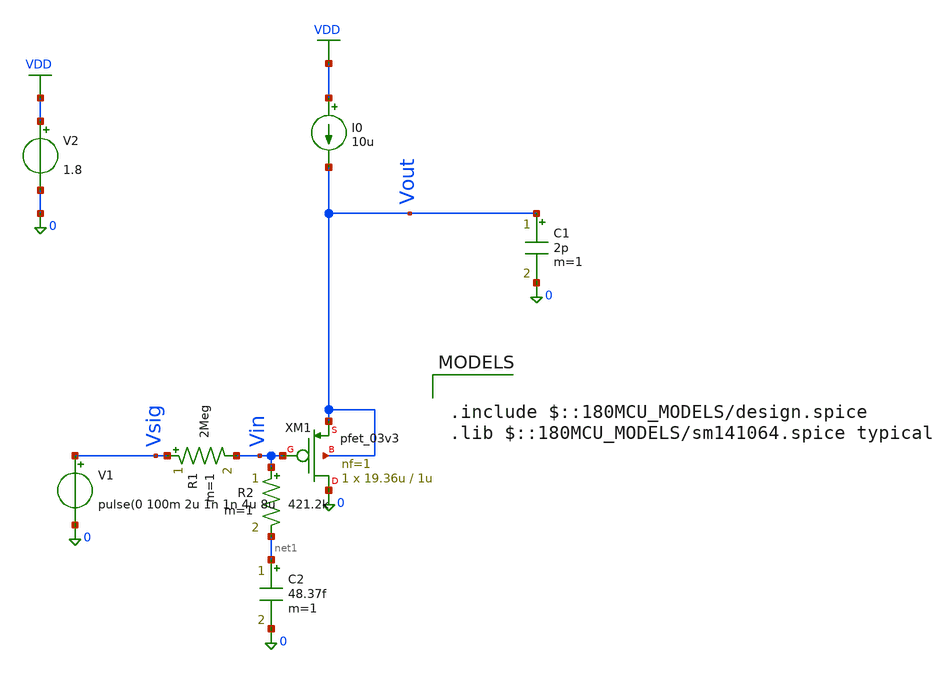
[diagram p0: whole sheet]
** sch_path: Lab_04/CD_comp.sch
**.subckt CD_comp
XM1 0 Vin Vout Vout pfet_03v3 L=1u W=19.36u nf=1 ad='int((nf+1)/2) * W/nf * 0.18u' as='int((nf+2)/2) * W/nf * 0.18u'
+ pd='2*int((nf+1)/2) * (W/nf + 0.18u)' ps='2*int((nf+2)/2) * (W/nf + 0.18u)' nrd='0.18u / W' nrs='0.18u / W'
+ sa=0 sb=0 sd=0 m=1
I0 VDD Vout 10u
V1 Vsig 0 pulse(0 100m 2u 1n 1n 4u 8u
R1 Vsig Vin 2Meg m=1
V2 VDD 0 1.8
C1 Vout 0 2p m=1
R2 Vin net1 421.2k m=1
C2 net1 0 48.37f m=1
**** begin user architecture code

.include $::180MCU_MODELS/design.spice
.lib $::180MCU_MODELS/sm141064.spice typical


.control
alterparam sw_stat_global = 0
alterparam sw_stat_mismatch = 0
reset
set outfile = overshoot_results.txt
tran 10n 10u
write cd_amp_comp.raw
set appendwrite
echo "CD Amplifier Transient Sim Results" > $outfile
foreach cap 2p 4p 8p
echo "Running Sim using Cap=$cap"
alter c1=$cap
tran 10n 10u
write cd_amp_comp.raw
meas tran vpeak MAX v(vout)
meas tran vfinal AVG v(vout) FROM=5.9u TO=6u
meas tran vinitial AVG v(vout) FROM=1u TO=1.1u
let overshoot_percent=(vpeak - vfinal)/(vfinal-vinitial) * 100
echo "CL = $cap, Overshoot (%) = $&overshoot_percent" >> $outfile
end
alter c1=2p
foreach my_res 20k 200k 2meg
echo "Running Sim using Res=$my_res"
alter r1=$my_res
tran 10n 10u
write cd_amp_comp.raw
meas tran vpeak MAX v(vout)
meas tran vfinal AVG v(vout) FROM=5.9u TO=6u
meas tran vinitial AVG v(vout) FROM=1u TO=1.1u
let overshoot_percent = (vpeak - vfinal)/(vfinal - vinitial) * 100
echo "Rsig = $my_res, Overshoot (%) = $&overshoot_percent" >> $outfile
end
.endc

**** end user architecture code
**.ends
.GLOBAL VDD
.end
